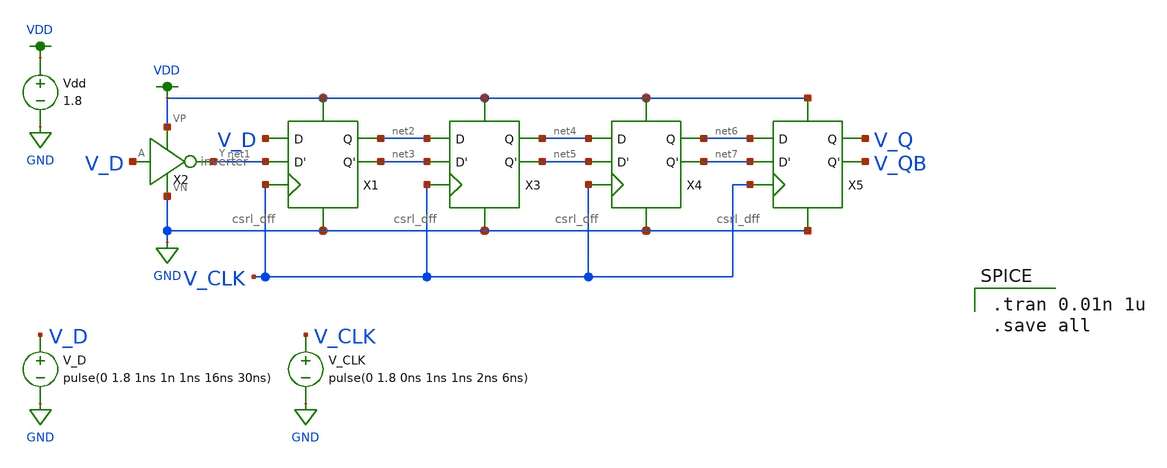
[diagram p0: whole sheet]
** sch_path: MP2/xschem/csrl_4reg_tran.sch
**.subckt csrl_4reg_tran
Vdd VDD GND 1.8
V_D V_D GND pulse(0 1.8 1ns 1n 1ns 16ns 30ns)
V_CLK V_CLK GND pulse(0 1.8 0ns 1ns 1ns 2ns 6ns)
X2 V_D net1 VDD GND inverter
X1 net1 V_CLK V_D net2 net3 VDD GND csrl_dff
X3 net3 V_CLK net2 net4 net5 VDD GND csrl_dff
X4 net5 V_CLK net4 net6 net7 VDD GND csrl_dff
X5 net7 V_CLK net6 V_Q V_QB VDD GND csrl_dff
**** begin user architecture code

.option wnflag=1
.lib ~/skywater/skywater-pdk/libraries/sky130_fd_pr_ngspice/latest/models/sky130.lib.spice tt


.tran 0.01n 1u
.save all

**** end user architecture code
**.ends
.GLOBAL VDD
.GLOBAL GND
.end
